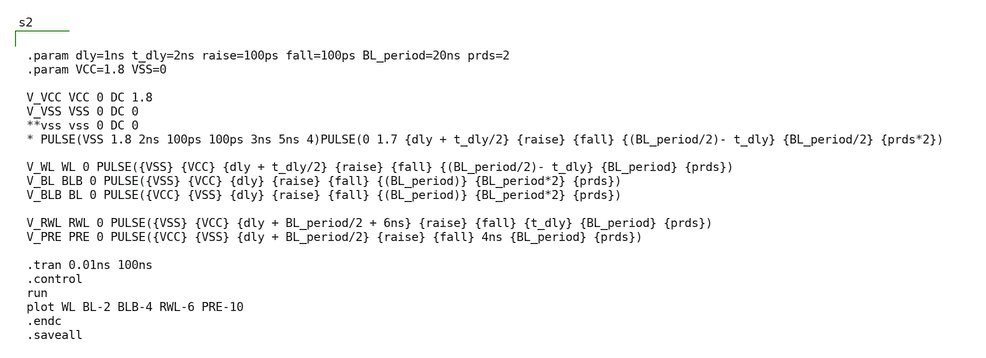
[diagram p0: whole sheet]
** sch_path: untitled.sch
**.subckt untitled
**** begin user architecture code


.param dly=1ns t_dly=2ns raise=100ps fall=100ps BL_period=20ns prds=2
.param VCC=1.8 VSS=0

V_VCC VCC 0 DC 1.8
V_VSS VSS 0 DC 0
**vss vss 0 DC 0
* PULSE(VSS 1.8 2ns 100ps 100ps 3ns 5ns 4)PULSE(0 1.7 {dly + t_dly/2} {raise} {fall} {(BL_period/2)- t_dly}
*+ {BL_period/2} {prds*2})

V_WL WL 0 PULSE({VSS} {VCC} {dly + t_dly/2} {raise} {fall} {(BL_period/2)- t_dly} {BL_period} {prds})
V_BL BLB 0 PULSE({VSS} {VCC} {dly} {raise} {fall} {(BL_period)} {BL_period*2} {prds})
V_BLB BL 0 PULSE({VCC} {VSS} {dly} {raise} {fall} {(BL_period)} {BL_period*2} {prds})

V_RWL RWL 0 PULSE({VSS} {VCC} {dly + BL_period/2 + 6ns} {raise} {fall} {t_dly} {BL_period} {prds})
V_PRE PRE 0 PULSE({VCC} {VSS} {dly + BL_period/2} {raise} {fall} 4ns {BL_period} {prds})

.tran 0.01ns 100ns
.control
run
plot WL BL-2 BLB-4 RWL-6 PRE-10
.endc
.saveall



**** end user architecture code
**.ends
.end
